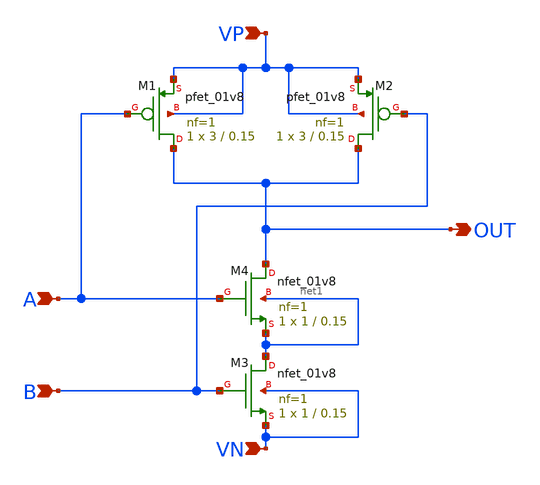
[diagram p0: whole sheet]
** sch_path: basic_cell/single_cell/nand/nand.sch
**.subckt nand OUT A B VN VP
*.opin OUT
*.ipin A
*.ipin B
*.ipin VN
*.ipin VP
XM4 OUT A net1 net1 sky130_fd_pr__nfet_01v8 L=0.15 W=1 nf=1 ad='int((nf+1)/2) * W/nf * 0.29' as='int((nf+2)/2) * W/nf * 0.29'
+ pd='2*int((nf+1)/2) * (W/nf + 0.29)' ps='2*int((nf+2)/2) * (W/nf + 0.29)' nrd='0.29 / W' nrs='0.29 / W'
+ sa=0 sb=0 sd=0 mult=1 m=1
XM3 net1 B VN VN sky130_fd_pr__nfet_01v8 L=0.15 W=1 nf=1 ad='int((nf+1)/2) * W/nf * 0.29' as='int((nf+2)/2) * W/nf * 0.29'
+ pd='2*int((nf+1)/2) * (W/nf + 0.29)' ps='2*int((nf+2)/2) * (W/nf + 0.29)' nrd='0.29 / W' nrs='0.29 / W'
+ sa=0 sb=0 sd=0 mult=1 m=1
XM1 OUT A VP VP sky130_fd_pr__pfet_01v8 L=0.15 W=3 nf=1 ad='int((nf+1)/2) * W/nf * 0.29' as='int((nf+2)/2) * W/nf * 0.29'
+ pd='2*int((nf+1)/2) * (W/nf + 0.29)' ps='2*int((nf+2)/2) * (W/nf + 0.29)' nrd='0.29 / W' nrs='0.29 / W'
+ sa=0 sb=0 sd=0 mult=1 m=1
XM2 OUT B VP VP sky130_fd_pr__pfet_01v8 L=0.15 W=3 nf=1 ad='int((nf+1)/2) * W/nf * 0.29' as='int((nf+2)/2) * W/nf * 0.29'
+ pd='2*int((nf+1)/2) * (W/nf + 0.29)' ps='2*int((nf+2)/2) * (W/nf + 0.29)' nrd='0.29 / W' nrs='0.29 / W'
+ sa=0 sb=0 sd=0 mult=1 m=1
**.ends
.end
